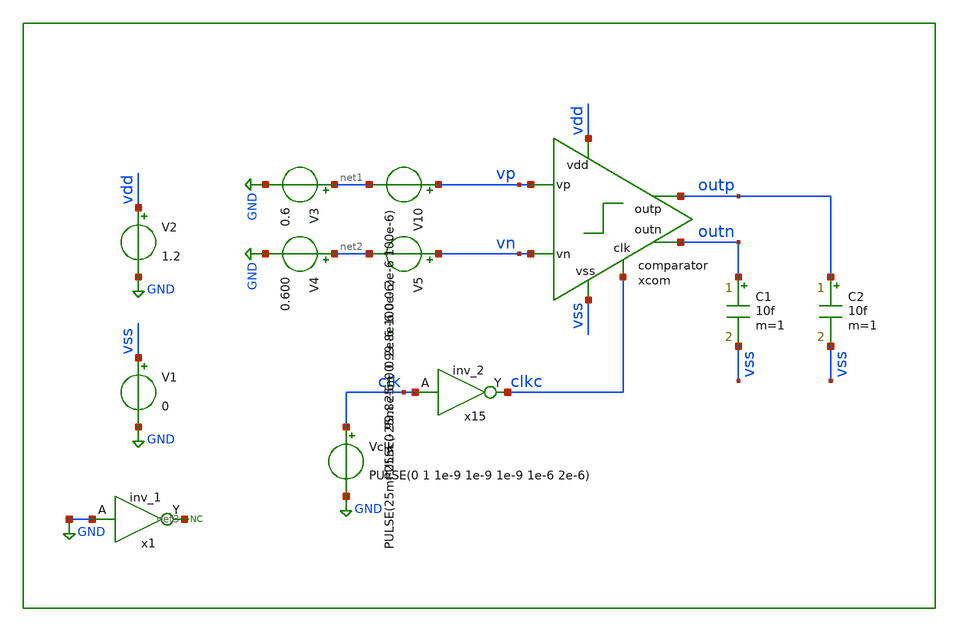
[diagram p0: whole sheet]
** sch_path: xschem/tb/comparator/tran_comparator.sch
**.subckt tran_comparator
xcom vss vdd clkc outp vp outn vn comparator
x15 clk vss vss vdd vdd clkc sky130_fd_sc_hd__inv_2
V1 vss GND 0
V2 vdd GND 1.2
C1 outn vss 10f m=1
C2 outp vss 10f m=1
Vclk clk GND PULSE(0 1 1e-9 1e-9 1e-9 1e-6 2e-6)
V3 net1 GND 0.6
V4 net2 GND 0.600
* noconn #net3
x1 GND vss vss vdd vdd net3 sky130_fd_sc_hd__inv_1
V10 vp net1 PULSE(-25m 25m 0 99.8e-6 0 0.2e-6 100e-6)
V5 vn net2 PULSE(25m -25m 0 99.8e-6 0 0.2e-6 100e-6)
**** begin user architecture code
[sky130_models]

*.include $::DESIGN_PATH/design/tb/comparator/ctl.sp

*vt0 trim_0_ 0 1.2
*vt1 trim_1_ 0 1.2
*vt2 trim_2_ 0 1.2
*vt3 trim_3_ 0 1.2
*vt4 trim_4_ 0 1.2

.options method trap

.control
.param MC_SWITCH=0

tran 100e-9 100e-6
plt outp
.endc


* FET CORNERS
.include $::SKYWATER_MODELS/models/corners/tt.spice
*.include $::SKYWATER_MODELS/corners/ff.spice
*.include $::SKYWATER_MODELS/corners/ss.spice
*.include $::SKYWATER_MODELS/corners/sf.spice
*.include $::SKYWATER_MODELS/corners/fs.spice

* TT + R + C
*.include $::SKYWATER_MODELS/corners/tt_rmax_cmax.spice
*.include $::SKYWATER_MODELS/corners/tt_rmin_cmin.spice
*.include $::SKYWATER_MODELS/corners/tt_rmax_cmin.spice
*.include $::SKYWATER_MODELS/corners/tt_rmin_cmax.spice

* FF + R + C
*.include $::SKYWATER_MODELS/corners/ff_rmax_cmax.spice
*.include $::SKYWATER_MODELS/corners/ff_rmin_cmin.spice
*.include $::SKYWATER_MODELS/corners/ff_rmax_cmin.spice
*.include $::SKYWATER_MODELS/corners/ff_rmin_cmax.spice


* SS + R + C
*.include $::SKYWATER_MODELS/corners/ss_rmax_cmax.spice
*.include $::SKYWATER_MODELS/corners/ss_rmin_cmin.spice
*.include $::SKYWATER_MODELS/corners/ss_rmax_cmin.spice
*.include $::SKYWATER_MODELS/corners/ss_rmin_cmax.spice

* SF + R + C
*.include $::SKYWATER_MODELS/corners/sf_rmax_cmax.spice
*.include $::SKYWATER_MODELS/corners/sf_rmin_cmin.spice
*.include $::SKYWATER_MODELS/corners/sf_rmax_cmin.spice
*.include $::SKYWATER_MODELS/corners/sf_rmin_cmax.spice

* FS + R + C
*.include $::SKYWATER_MODELS/corners/fs_rmax_cmax.spice
*.include $::SKYWATER_MODELS/corners/fs_rmin_cmin.spice
*.include $::SKYWATER_MODELS/corners/fs_rmax_cmin.spice
*.include $::SKYWATER_MODELS/corners/fs_rmin_cmax.spice

**** end user architecture code
**.ends

* expanding   symbol:  sar_10b/comparator/comparator.sym # of pins=7
** sym_path: xschem/sar_10b/comparator/comparator.sym
** sch_path: xschem/sar_10b/comparator/comparator.sch
.subckt comparator vss vdd clk outp vp outn vn
*.ipin vn
*.ipin vp
*.ipin clk
*.iopin vdd
*.iopin vss
*.opin outp
*.opin outn
XMdiff diff clk vss vss sky130_fd_pr__nfet_01v8 L=0.3 W=1 nf=1 ad='int((nf+1)/2) * W/nf * 0.29' as='int((nf+2)/2) * W/nf * 0.29'
+ pd='2*int((nf+1)/2) * (W/nf + 0.29)' ps='2*int((nf+2)/2) * (W/nf + 0.29)' nrd='0.29 / W' nrs='0.29 / W'
+ sa=0 sb=0 sd=0 mult=2 m=2
XMinn net1 vn diff vss sky130_fd_pr__nfet_01v8 L=0.3 W=1 nf=1 ad='int((nf+1)/2) * W/nf * 0.29' as='int((nf+2)/2) * W/nf * 0.29'
+ pd='2*int((nf+1)/2) * (W/nf + 0.29)' ps='2*int((nf+2)/2) * (W/nf + 0.29)' nrd='0.29 / W' nrs='0.29 / W'
+ sa=0 sb=0 sd=0 mult=1 m=1
XMinp net2 vp diff vss sky130_fd_pr__nfet_01v8 L=0.3 W=1 nf=1 ad='int((nf+1)/2) * W/nf * 0.29' as='int((nf+2)/2) * W/nf * 0.29'
+ pd='2*int((nf+1)/2) * (W/nf + 0.29)' ps='2*int((nf+2)/2) * (W/nf + 0.29)' nrd='0.29 / W' nrs='0.29 / W'
+ sa=0 sb=0 sd=0 mult=1 m=1
XMl4 outp outn vdd vdd sky130_fd_pr__pfet_01v8 L=0.3 W=1 nf=1 ad='int((nf+1)/2) * W/nf * 0.29' as='int((nf+2)/2) * W/nf * 0.29'
+ pd='2*int((nf+1)/2) * (W/nf + 0.29)' ps='2*int((nf+2)/2) * (W/nf + 0.29)' nrd='0.29 / W' nrs='0.29 / W'
+ sa=0 sb=0 sd=0 mult=1 m=1
XMl3 outn outp vdd vdd sky130_fd_pr__pfet_01v8 L=0.3 W=1 nf=1 ad='int((nf+1)/2) * W/nf * 0.29' as='int((nf+2)/2) * W/nf * 0.29'
+ pd='2*int((nf+1)/2) * (W/nf + 0.29)' ps='2*int((nf+2)/2) * (W/nf + 0.29)' nrd='0.29 / W' nrs='0.29 / W'
+ sa=0 sb=0 sd=0 mult=1 m=1
XM3 outp clk vdd vdd sky130_fd_pr__pfet_01v8 L=0.3 W=1 nf=1 ad='int((nf+1)/2) * W/nf * 0.29' as='int((nf+2)/2) * W/nf * 0.29'
+ pd='2*int((nf+1)/2) * (W/nf + 0.29)' ps='2*int((nf+2)/2) * (W/nf + 0.29)' nrd='0.29 / W' nrs='0.29 / W'
+ sa=0 sb=0 sd=0 mult=1 m=1
XM2 outn clk vdd vdd sky130_fd_pr__pfet_01v8 L=0.3 W=1 nf=1 ad='int((nf+1)/2) * W/nf * 0.29' as='int((nf+2)/2) * W/nf * 0.29'
+ pd='2*int((nf+1)/2) * (W/nf + 0.29)' ps='2*int((nf+2)/2) * (W/nf + 0.29)' nrd='0.29 / W' nrs='0.29 / W'
+ sa=0 sb=0 sd=0 mult=1 m=1
XMl1 outn outp net1 vss sky130_fd_pr__nfet_01v8 L=0.3 W=1 nf=1 ad='int((nf+1)/2) * W/nf * 0.29' as='int((nf+2)/2) * W/nf * 0.29'
+ pd='2*int((nf+1)/2) * (W/nf + 0.29)' ps='2*int((nf+2)/2) * (W/nf + 0.29)' nrd='0.29 / W' nrs='0.29 / W'
+ sa=0 sb=0 sd=0 mult=1 m=1
XMl2 outp outn net2 vss sky130_fd_pr__nfet_01v8 L=0.3 W=1 nf=1 ad='int((nf+1)/2) * W/nf * 0.29' as='int((nf+2)/2) * W/nf * 0.29'
+ pd='2*int((nf+1)/2) * (W/nf + 0.29)' ps='2*int((nf+2)/2) * (W/nf + 0.29)' nrd='0.29 / W' nrs='0.29 / W'
+ sa=0 sb=0 sd=0 mult=1 m=1
.ends

.GLOBAL GND
.end
